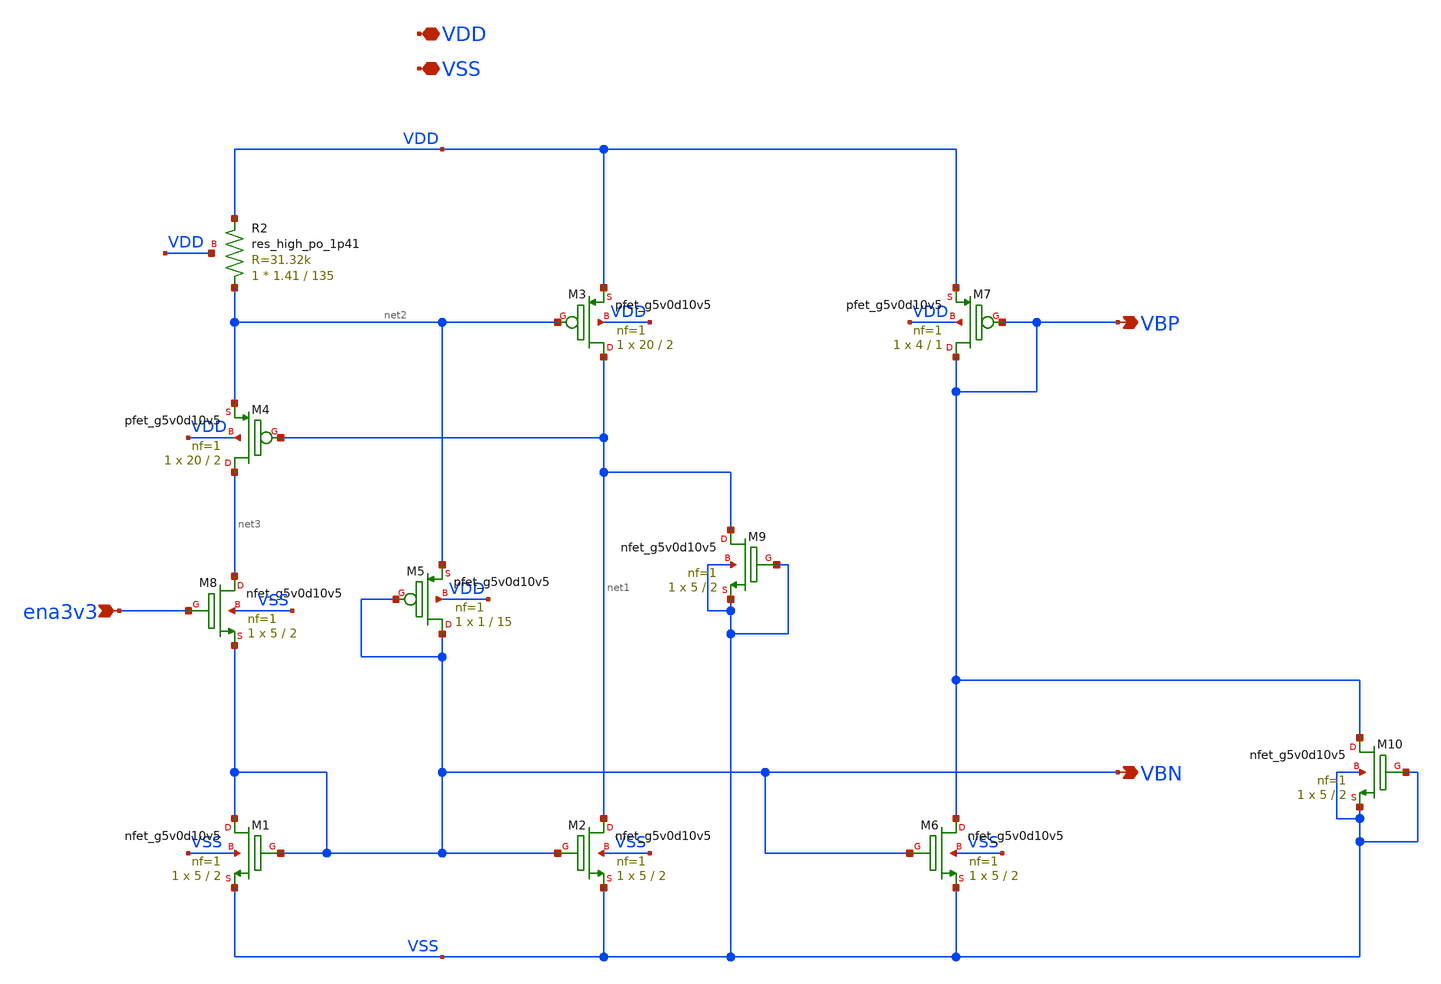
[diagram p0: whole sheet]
** sch_path: xschem/comparator_bias.sch
**.subckt comparator_bias VBP VBN VDD VSS ena3v3
*.opin VBP
*.opin VBN
*.iopin VDD
*.iopin VSS
*.ipin ena3v3
XM3 net1 net2 VDD VDD sky130_fd_pr__pfet_g5v0d10v5 L=2 W=20 nf=1 ad='int((nf+1)/2) * W/nf * 0.29' as='int((nf+2)/2) * W/nf * 0.29'
+ pd='2*int((nf+1)/2) * (W/nf + 0.29)' ps='2*int((nf+2)/2) * (W/nf + 0.29)' nrd='0.29 / W' nrs='0.29 / W'
+ sa=0 sb=0 sd=0 mult=1 m=1
XM4 net3 net1 net2 VDD sky130_fd_pr__pfet_g5v0d10v5 L=2 W=20 nf=1 ad='int((nf+1)/2) * W/nf * 0.29' as='int((nf+2)/2) * W/nf * 0.29'
+ pd='2*int((nf+1)/2) * (W/nf + 0.29)' ps='2*int((nf+2)/2) * (W/nf + 0.29)' nrd='0.29 / W' nrs='0.29 / W'
+ sa=0 sb=0 sd=0 mult=1 m=1
XM5 VBN VBN net2 VDD sky130_fd_pr__pfet_g5v0d10v5 L=15 W=1 nf=1 ad='int((nf+1)/2) * W/nf * 0.29' as='int((nf+2)/2) * W/nf * 0.29'
+ pd='2*int((nf+1)/2) * (W/nf + 0.29)' ps='2*int((nf+2)/2) * (W/nf + 0.29)' nrd='0.29 / W' nrs='0.29 / W'
+ sa=0 sb=0 sd=0 mult=1 m=1
XM7 VBP VBP VDD VDD sky130_fd_pr__pfet_g5v0d10v5 L=1 W=4 nf=1 ad='int((nf+1)/2) * W/nf * 0.29' as='int((nf+2)/2) * W/nf * 0.29'
+ pd='2*int((nf+1)/2) * (W/nf + 0.29)' ps='2*int((nf+2)/2) * (W/nf + 0.29)' nrd='0.29 / W' nrs='0.29 / W'
+ sa=0 sb=0 sd=0 mult=1 m=1
XM1 VBN VBN VSS VSS sky130_fd_pr__nfet_g5v0d10v5 L=2 W=5 nf=1 ad='int((nf+1)/2) * W/nf * 0.29' as='int((nf+2)/2) * W/nf * 0.29'
+ pd='2*int((nf+1)/2) * (W/nf + 0.29)' ps='2*int((nf+2)/2) * (W/nf + 0.29)' nrd='0.29 / W' nrs='0.29 / W'
+ sa=0 sb=0 sd=0 mult=1 m=1
XM2 net1 VBN VSS VSS sky130_fd_pr__nfet_g5v0d10v5 L=2 W=5 nf=1 ad='int((nf+1)/2) * W/nf * 0.29' as='int((nf+2)/2) * W/nf * 0.29'
+ pd='2*int((nf+1)/2) * (W/nf + 0.29)' ps='2*int((nf+2)/2) * (W/nf + 0.29)' nrd='0.29 / W' nrs='0.29 / W'
+ sa=0 sb=0 sd=0 mult=1 m=1
XM6 VBP VBN VSS VSS sky130_fd_pr__nfet_g5v0d10v5 L=2 W=5 nf=1 ad='int((nf+1)/2) * W/nf * 0.29' as='int((nf+2)/2) * W/nf * 0.29'
+ pd='2*int((nf+1)/2) * (W/nf + 0.29)' ps='2*int((nf+2)/2) * (W/nf + 0.29)' nrd='0.29 / W' nrs='0.29 / W'
+ sa=0 sb=0 sd=0 mult=1 m=1
XM8 net3 ena3v3 VBN VSS sky130_fd_pr__nfet_g5v0d10v5 L=2 W=5 nf=1 ad='int((nf+1)/2) * W/nf * 0.29' as='int((nf+2)/2) * W/nf * 0.29'
+ pd='2*int((nf+1)/2) * (W/nf + 0.29)' ps='2*int((nf+2)/2) * (W/nf + 0.29)' nrd='0.29 / W' nrs='0.29 / W'
+ sa=0 sb=0 sd=0 mult=1 m=1
XM9 net1 VSS VSS VSS sky130_fd_pr__nfet_g5v0d10v5 L=2 W=5 nf=1 ad='int((nf+1)/2) * W/nf * 0.29' as='int((nf+2)/2) * W/nf * 0.29'
+ pd='2*int((nf+1)/2) * (W/nf + 0.29)' ps='2*int((nf+2)/2) * (W/nf + 0.29)' nrd='0.29 / W' nrs='0.29 / W'
+ sa=0 sb=0 sd=0 mult=1 m=1
XM10 VBP VSS VSS VSS sky130_fd_pr__nfet_g5v0d10v5 L=2 W=5 nf=1 ad='int((nf+1)/2) * W/nf * 0.29' as='int((nf+2)/2) * W/nf * 0.29'
+ pd='2*int((nf+1)/2) * (W/nf + 0.29)' ps='2*int((nf+2)/2) * (W/nf + 0.29)' nrd='0.29 / W' nrs='0.29 / W'
+ sa=0 sb=0 sd=0 mult=1 m=1
XR2 net2 VDD VDD sky130_fd_pr__res_high_po_1p41 L=135 mult=1 m=1
**.ends
.end
